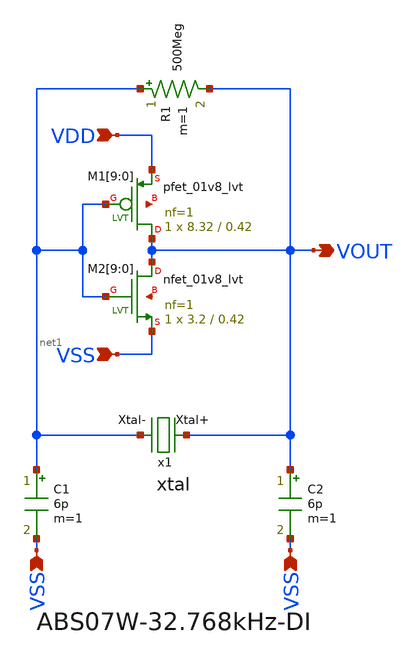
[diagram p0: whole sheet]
** sch_path: design/THESIS_EXP_RO_INVERTER_SKY130A/xtal_osc.sch
**.subckt xtal_osc VDD VSS VSS VSS VOUT
*.ipin VDD
*.ipin VSS
*.ipin VSS
*.ipin VSS
*.opin VOUT
x1 VOUT net1 xtal
C1 net1 VSS 6p m=1
C2 VOUT VSS 6p m=1
R1 net1 VOUT 500Meg m=1
XM1[9] VOUT net1 VDD net2[9] sky130_fd_pr__pfet_01v8_lvt L=0.42 W=8.32 nf=1 ad='int((nf+1)/2) * W/nf * 0.29'
+ as='int((nf+2)/2) * W/nf * 0.29' pd='2*int((nf+1)/2) * (W/nf + 0.29)' ps='2*int((nf+2)/2) * (W/nf + 0.29)'
+ nrd='0.29 / W' nrs='0.29 / W' sa=0 sb=0 sd=0 mult=1 m=1
XM1[8] VOUT net1 VDD net2[8] sky130_fd_pr__pfet_01v8_lvt L=0.42 W=8.32 nf=1 ad='int((nf+1)/2) * W/nf * 0.29'
+ as='int((nf+2)/2) * W/nf * 0.29' pd='2*int((nf+1)/2) * (W/nf + 0.29)' ps='2*int((nf+2)/2) * (W/nf + 0.29)'
+ nrd='0.29 / W' nrs='0.29 / W' sa=0 sb=0 sd=0 mult=1 m=1
XM1[7] VOUT net1 VDD net2[7] sky130_fd_pr__pfet_01v8_lvt L=0.42 W=8.32 nf=1 ad='int((nf+1)/2) * W/nf * 0.29'
+ as='int((nf+2)/2) * W/nf * 0.29' pd='2*int((nf+1)/2) * (W/nf + 0.29)' ps='2*int((nf+2)/2) * (W/nf + 0.29)'
+ nrd='0.29 / W' nrs='0.29 / W' sa=0 sb=0 sd=0 mult=1 m=1
XM1[6] VOUT net1 VDD net2[6] sky130_fd_pr__pfet_01v8_lvt L=0.42 W=8.32 nf=1 ad='int((nf+1)/2) * W/nf * 0.29'
+ as='int((nf+2)/2) * W/nf * 0.29' pd='2*int((nf+1)/2) * (W/nf + 0.29)' ps='2*int((nf+2)/2) * (W/nf + 0.29)'
+ nrd='0.29 / W' nrs='0.29 / W' sa=0 sb=0 sd=0 mult=1 m=1
XM1[5] VOUT net1 VDD net2[5] sky130_fd_pr__pfet_01v8_lvt L=0.42 W=8.32 nf=1 ad='int((nf+1)/2) * W/nf * 0.29'
+ as='int((nf+2)/2) * W/nf * 0.29' pd='2*int((nf+1)/2) * (W/nf + 0.29)' ps='2*int((nf+2)/2) * (W/nf + 0.29)'
+ nrd='0.29 / W' nrs='0.29 / W' sa=0 sb=0 sd=0 mult=1 m=1
XM1[4] VOUT net1 VDD net2[4] sky130_fd_pr__pfet_01v8_lvt L=0.42 W=8.32 nf=1 ad='int((nf+1)/2) * W/nf * 0.29'
+ as='int((nf+2)/2) * W/nf * 0.29' pd='2*int((nf+1)/2) * (W/nf + 0.29)' ps='2*int((nf+2)/2) * (W/nf + 0.29)'
+ nrd='0.29 / W' nrs='0.29 / W' sa=0 sb=0 sd=0 mult=1 m=1
XM1[3] VOUT net1 VDD net2[3] sky130_fd_pr__pfet_01v8_lvt L=0.42 W=8.32 nf=1 ad='int((nf+1)/2) * W/nf * 0.29'
+ as='int((nf+2)/2) * W/nf * 0.29' pd='2*int((nf+1)/2) * (W/nf + 0.29)' ps='2*int((nf+2)/2) * (W/nf + 0.29)'
+ nrd='0.29 / W' nrs='0.29 / W' sa=0 sb=0 sd=0 mult=1 m=1
XM1[2] VOUT net1 VDD net2[2] sky130_fd_pr__pfet_01v8_lvt L=0.42 W=8.32 nf=1 ad='int((nf+1)/2) * W/nf * 0.29'
+ as='int((nf+2)/2) * W/nf * 0.29' pd='2*int((nf+1)/2) * (W/nf + 0.29)' ps='2*int((nf+2)/2) * (W/nf + 0.29)'
+ nrd='0.29 / W' nrs='0.29 / W' sa=0 sb=0 sd=0 mult=1 m=1
XM1[1] VOUT net1 VDD net2[1] sky130_fd_pr__pfet_01v8_lvt L=0.42 W=8.32 nf=1 ad='int((nf+1)/2) * W/nf * 0.29'
+ as='int((nf+2)/2) * W/nf * 0.29' pd='2*int((nf+1)/2) * (W/nf + 0.29)' ps='2*int((nf+2)/2) * (W/nf + 0.29)'
+ nrd='0.29 / W' nrs='0.29 / W' sa=0 sb=0 sd=0 mult=1 m=1
XM1[0] VOUT net1 VDD net2[0] sky130_fd_pr__pfet_01v8_lvt L=0.42 W=8.32 nf=1 ad='int((nf+1)/2) * W/nf * 0.29'
+ as='int((nf+2)/2) * W/nf * 0.29' pd='2*int((nf+1)/2) * (W/nf + 0.29)' ps='2*int((nf+2)/2) * (W/nf + 0.29)'
+ nrd='0.29 / W' nrs='0.29 / W' sa=0 sb=0 sd=0 mult=1 m=1
XM2[9] VOUT net1 VSS net3[9] sky130_fd_pr__nfet_01v8_lvt L=0.42 W=3.2 nf=1 ad='int((nf+1)/2) * W/nf * 0.29'
+ as='int((nf+2)/2) * W/nf * 0.29' pd='2*int((nf+1)/2) * (W/nf + 0.29)' ps='2*int((nf+2)/2) * (W/nf + 0.29)'
+ nrd='0.29 / W' nrs='0.29 / W' sa=0 sb=0 sd=0 mult=1 m=1
XM2[8] VOUT net1 VSS net3[8] sky130_fd_pr__nfet_01v8_lvt L=0.42 W=3.2 nf=1 ad='int((nf+1)/2) * W/nf * 0.29'
+ as='int((nf+2)/2) * W/nf * 0.29' pd='2*int((nf+1)/2) * (W/nf + 0.29)' ps='2*int((nf+2)/2) * (W/nf + 0.29)'
+ nrd='0.29 / W' nrs='0.29 / W' sa=0 sb=0 sd=0 mult=1 m=1
XM2[7] VOUT net1 VSS net3[7] sky130_fd_pr__nfet_01v8_lvt L=0.42 W=3.2 nf=1 ad='int((nf+1)/2) * W/nf * 0.29'
+ as='int((nf+2)/2) * W/nf * 0.29' pd='2*int((nf+1)/2) * (W/nf + 0.29)' ps='2*int((nf+2)/2) * (W/nf + 0.29)'
+ nrd='0.29 / W' nrs='0.29 / W' sa=0 sb=0 sd=0 mult=1 m=1
XM2[6] VOUT net1 VSS net3[6] sky130_fd_pr__nfet_01v8_lvt L=0.42 W=3.2 nf=1 ad='int((nf+1)/2) * W/nf * 0.29'
+ as='int((nf+2)/2) * W/nf * 0.29' pd='2*int((nf+1)/2) * (W/nf + 0.29)' ps='2*int((nf+2)/2) * (W/nf + 0.29)'
+ nrd='0.29 / W' nrs='0.29 / W' sa=0 sb=0 sd=0 mult=1 m=1
XM2[5] VOUT net1 VSS net3[5] sky130_fd_pr__nfet_01v8_lvt L=0.42 W=3.2 nf=1 ad='int((nf+1)/2) * W/nf * 0.29'
+ as='int((nf+2)/2) * W/nf * 0.29' pd='2*int((nf+1)/2) * (W/nf + 0.29)' ps='2*int((nf+2)/2) * (W/nf + 0.29)'
+ nrd='0.29 / W' nrs='0.29 / W' sa=0 sb=0 sd=0 mult=1 m=1
XM2[4] VOUT net1 VSS net3[4] sky130_fd_pr__nfet_01v8_lvt L=0.42 W=3.2 nf=1 ad='int((nf+1)/2) * W/nf * 0.29'
+ as='int((nf+2)/2) * W/nf * 0.29' pd='2*int((nf+1)/2) * (W/nf + 0.29)' ps='2*int((nf+2)/2) * (W/nf + 0.29)'
+ nrd='0.29 / W' nrs='0.29 / W' sa=0 sb=0 sd=0 mult=1 m=1
XM2[3] VOUT net1 VSS net3[3] sky130_fd_pr__nfet_01v8_lvt L=0.42 W=3.2 nf=1 ad='int((nf+1)/2) * W/nf * 0.29'
+ as='int((nf+2)/2) * W/nf * 0.29' pd='2*int((nf+1)/2) * (W/nf + 0.29)' ps='2*int((nf+2)/2) * (W/nf + 0.29)'
+ nrd='0.29 / W' nrs='0.29 / W' sa=0 sb=0 sd=0 mult=1 m=1
XM2[2] VOUT net1 VSS net3[2] sky130_fd_pr__nfet_01v8_lvt L=0.42 W=3.2 nf=1 ad='int((nf+1)/2) * W/nf * 0.29'
+ as='int((nf+2)/2) * W/nf * 0.29' pd='2*int((nf+1)/2) * (W/nf + 0.29)' ps='2*int((nf+2)/2) * (W/nf + 0.29)'
+ nrd='0.29 / W' nrs='0.29 / W' sa=0 sb=0 sd=0 mult=1 m=1
XM2[1] VOUT net1 VSS net3[1] sky130_fd_pr__nfet_01v8_lvt L=0.42 W=3.2 nf=1 ad='int((nf+1)/2) * W/nf * 0.29'
+ as='int((nf+2)/2) * W/nf * 0.29' pd='2*int((nf+1)/2) * (W/nf + 0.29)' ps='2*int((nf+2)/2) * (W/nf + 0.29)'
+ nrd='0.29 / W' nrs='0.29 / W' sa=0 sb=0 sd=0 mult=1 m=1
XM2[0] VOUT net1 VSS net3[0] sky130_fd_pr__nfet_01v8_lvt L=0.42 W=3.2 nf=1 ad='int((nf+1)/2) * W/nf * 0.29'
+ as='int((nf+2)/2) * W/nf * 0.29' pd='2*int((nf+1)/2) * (W/nf + 0.29)' ps='2*int((nf+2)/2) * (W/nf + 0.29)'
+ nrd='0.29 / W' nrs='0.29 / W' sa=0 sb=0 sd=0 mult=1 m=1
**.ends

* expanding   symbol:  THESIS_EXP_RO_INVERTER_SKY130A/xtal.sym # of pins=2
** sym_path: design/THESIS_EXP_RO_INVERTER_SKY130A/xtal.sym
** sch_path: design/THESIS_EXP_RO_INVERTER_SKY130A/xtal.sch
.subckt xtal Xtal+ Xtal-
*.iopin Xtal+
*.iopin Xtal-
R1 Xtal+ net1 38.194k m=1
C1 net1 net2 4.68f m=1
L1 net2 Xtal- 5048.571 m=1
C2 Xtal+ Xtal- 1.15p m=1
.ends

.end
